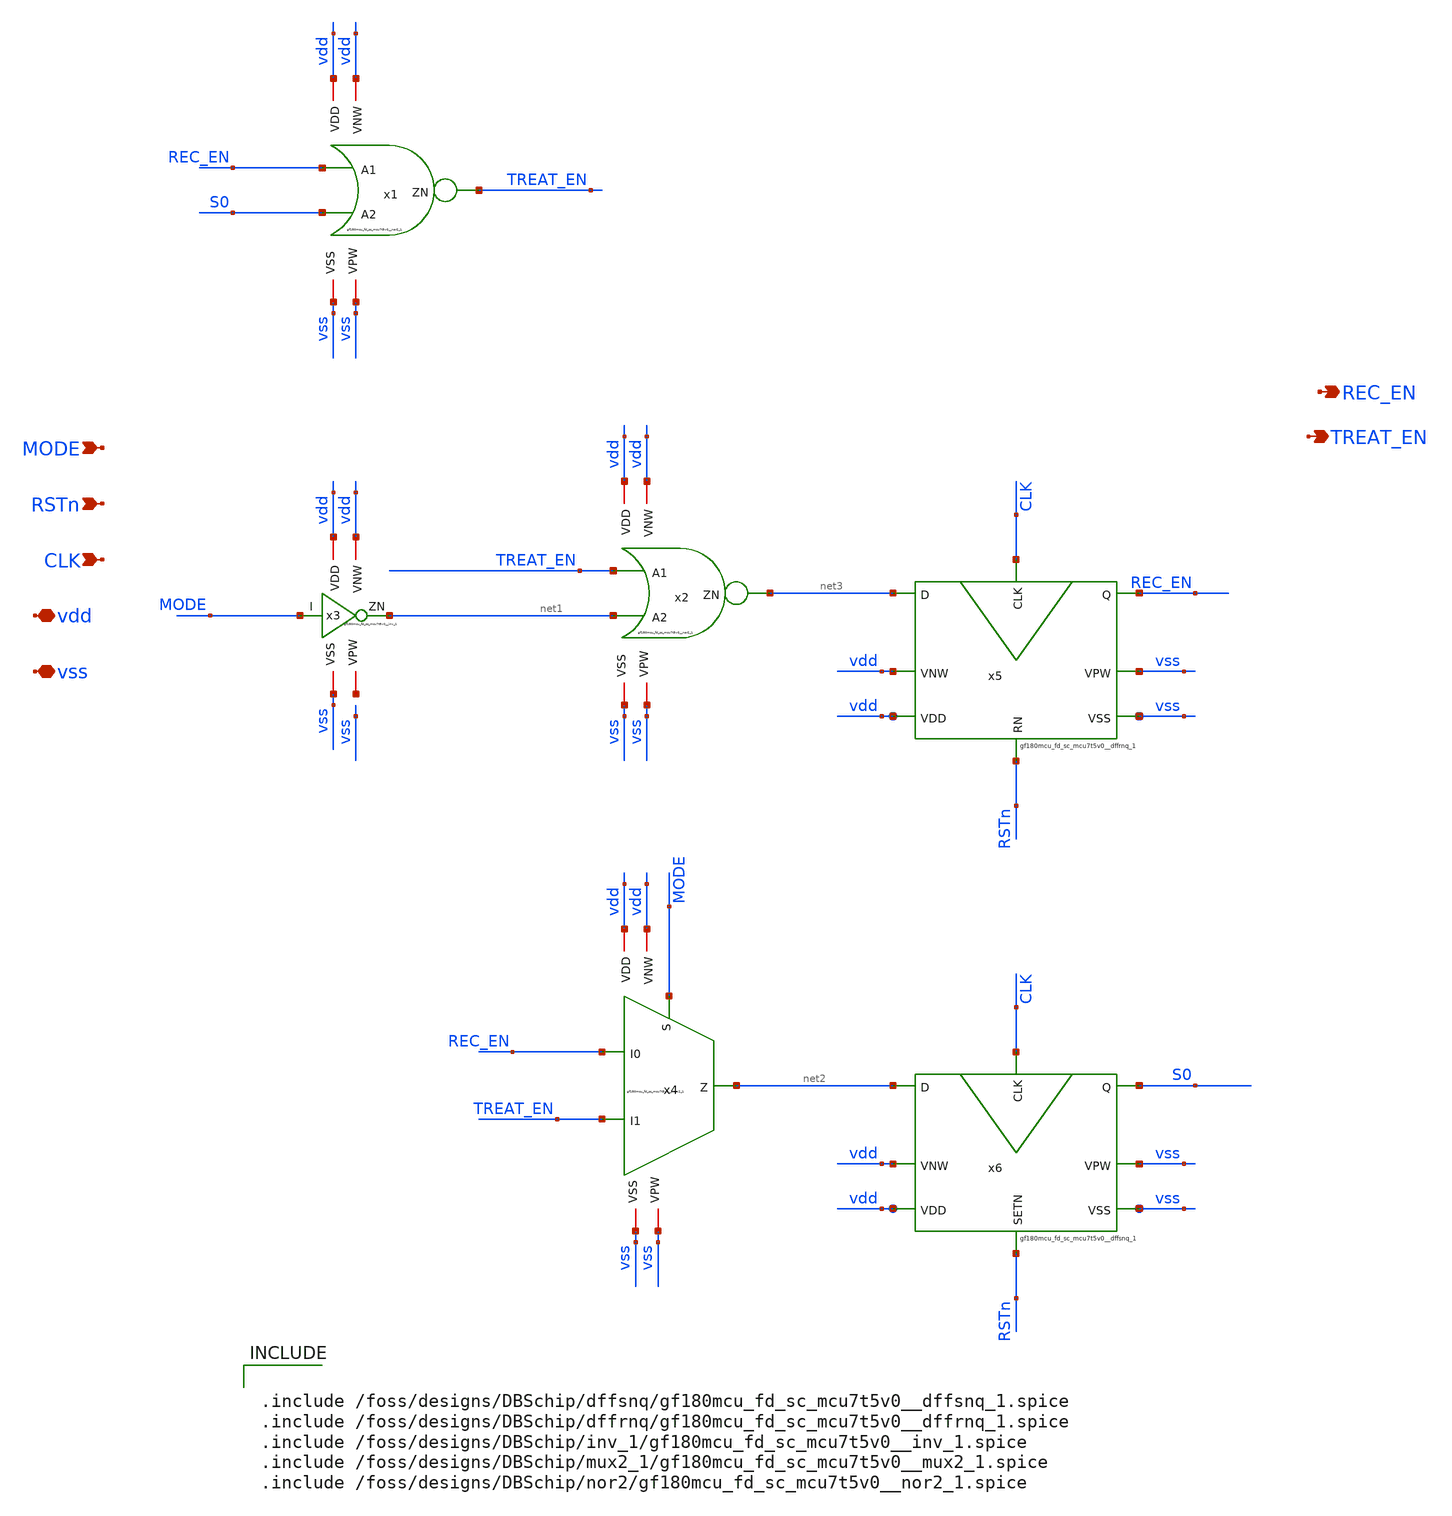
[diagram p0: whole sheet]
** sch_path: FSM/FSM.sch
**.subckt FSM REC_EN MODE RSTn CLK TREAT_EN vdd vss
*.opin REC_EN
*.ipin MODE
*.ipin RSTn
*.ipin CLK
*.opin TREAT_EN
*.iopin vdd
*.iopin vss
x1 REC_EN S0 TREAT_EN vdd vdd vss vss gf180mcu_fd_sc_mcu7t5v0__nor2_1
x2 TREAT_EN net1 net3 vdd vdd vss vss gf180mcu_fd_sc_mcu7t5v0__nor2_1
x3 MODE net1 vdd vdd net4 vss gf180mcu_fd_sc_mcu7t5v0__inv_1
x4 REC_EN TREAT_EN MODE net2 vdd vdd vss vss gf180mcu_fd_sc_mcu7t5v0__mux2_1
x5 net3 RSTn CLK REC_EN vdd vdd vss vss gf180mcu_fd_sc_mcu7t5v0__dffrnq_1
x6 net2 RSTn CLK S0 vdd vdd vss vss gf180mcu_fd_sc_mcu7t5v0__dffsnq_1
**** begin user architecture code


.include /foss/designs/DBSchip/dffsnq/gf180mcu_fd_sc_mcu7t5v0__dffsnq_1.spice
.include /foss/designs/DBSchip/dffrnq/gf180mcu_fd_sc_mcu7t5v0__dffrnq_1.spice
.include /foss/designs/DBSchip/inv_1/gf180mcu_fd_sc_mcu7t5v0__inv_1.spice
.include /foss/designs/DBSchip/mux2_1/gf180mcu_fd_sc_mcu7t5v0__mux2_1.spice
.include /foss/designs/DBSchip/nor2/gf180mcu_fd_sc_mcu7t5v0__nor2_1.spice


**** end user architecture code
**.ends
.end
